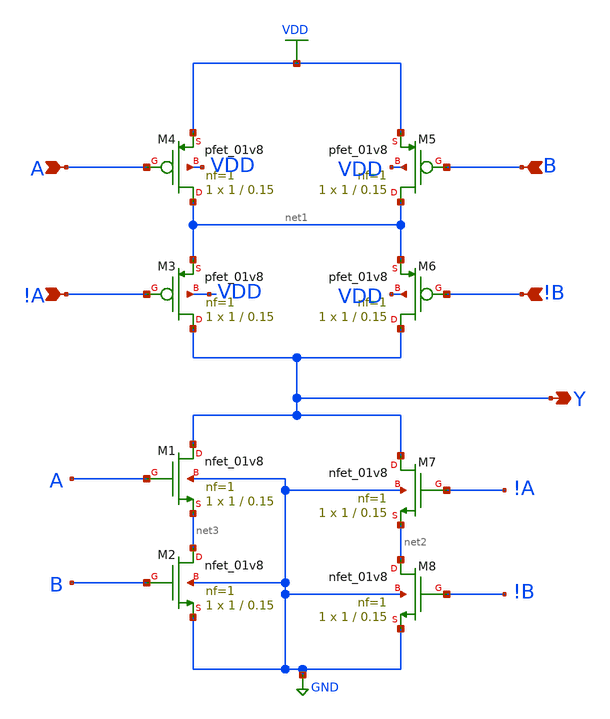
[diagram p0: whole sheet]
** sch_path: gates/No_inv_XOR2.sch
**.subckt No_inv_XOR2 A B Y !A !B
*.ipin A
*.ipin B
*.opin Y
*.ipin !A
*.ipin !B
XM1 Y A net3 GND sky130_fd_pr__nfet_01v8 L=0.15 W=1 nf=1 ad='int((nf+1)/2) * W/nf * 0.29' as='int((nf+2)/2) * W/nf * 0.29'
+ pd='2*int((nf+1)/2) * (W/nf + 0.29)' ps='2*int((nf+2)/2) * (W/nf + 0.29)' nrd='0.29 / W' nrs='0.29 / W'
+ sa=0 sb=0 sd=0 mult=1 m=1
XM2 net3 B GND GND sky130_fd_pr__nfet_01v8 L=0.15 W=1 nf=1 ad='int((nf+1)/2) * W/nf * 0.29' as='int((nf+2)/2) * W/nf * 0.29'
+ pd='2*int((nf+1)/2) * (W/nf + 0.29)' ps='2*int((nf+2)/2) * (W/nf + 0.29)' nrd='0.29 / W' nrs='0.29 / W'
+ sa=0 sb=0 sd=0 mult=1 m=1
XM3 Y !A net1 VDD sky130_fd_pr__pfet_01v8 L=0.15 W=1 nf=1 ad='int((nf+1)/2) * W/nf * 0.29' as='int((nf+2)/2) * W/nf * 0.29'
+ pd='2*int((nf+1)/2) * (W/nf + 0.29)' ps='2*int((nf+2)/2) * (W/nf + 0.29)' nrd='0.29 / W' nrs='0.29 / W'
+ sa=0 sb=0 sd=0 mult=1 m=1
XM4 net1 A VDD VDD sky130_fd_pr__pfet_01v8 L=0.15 W=1 nf=1 ad='int((nf+1)/2) * W/nf * 0.29' as='int((nf+2)/2) * W/nf * 0.29'
+ pd='2*int((nf+1)/2) * (W/nf + 0.29)' ps='2*int((nf+2)/2) * (W/nf + 0.29)' nrd='0.29 / W' nrs='0.29 / W'
+ sa=0 sb=0 sd=0 mult=1 m=1
XM5 net1 B VDD VDD sky130_fd_pr__pfet_01v8 L=0.15 W=1 nf=1 ad='int((nf+1)/2) * W/nf * 0.29' as='int((nf+2)/2) * W/nf * 0.29'
+ pd='2*int((nf+1)/2) * (W/nf + 0.29)' ps='2*int((nf+2)/2) * (W/nf + 0.29)' nrd='0.29 / W' nrs='0.29 / W'
+ sa=0 sb=0 sd=0 mult=1 m=1
XM6 Y !B net1 VDD sky130_fd_pr__pfet_01v8 L=0.15 W=1 nf=1 ad='int((nf+1)/2) * W/nf * 0.29' as='int((nf+2)/2) * W/nf * 0.29'
+ pd='2*int((nf+1)/2) * (W/nf + 0.29)' ps='2*int((nf+2)/2) * (W/nf + 0.29)' nrd='0.29 / W' nrs='0.29 / W'
+ sa=0 sb=0 sd=0 mult=1 m=1
XM7 Y !A net2 GND sky130_fd_pr__nfet_01v8 L=0.15 W=1 nf=1 ad='int((nf+1)/2) * W/nf * 0.29' as='int((nf+2)/2) * W/nf * 0.29'
+ pd='2*int((nf+1)/2) * (W/nf + 0.29)' ps='2*int((nf+2)/2) * (W/nf + 0.29)' nrd='0.29 / W' nrs='0.29 / W'
+ sa=0 sb=0 sd=0 mult=1 m=1
XM8 net2 !B GND GND sky130_fd_pr__nfet_01v8 L=0.15 W=1 nf=1 ad='int((nf+1)/2) * W/nf * 0.29' as='int((nf+2)/2) * W/nf * 0.29'
+ pd='2*int((nf+1)/2) * (W/nf + 0.29)' ps='2*int((nf+2)/2) * (W/nf + 0.29)' nrd='0.29 / W' nrs='0.29 / W'
+ sa=0 sb=0 sd=0 mult=1 m=1
**.ends
.GLOBAL VDD
.GLOBAL GND
.end
